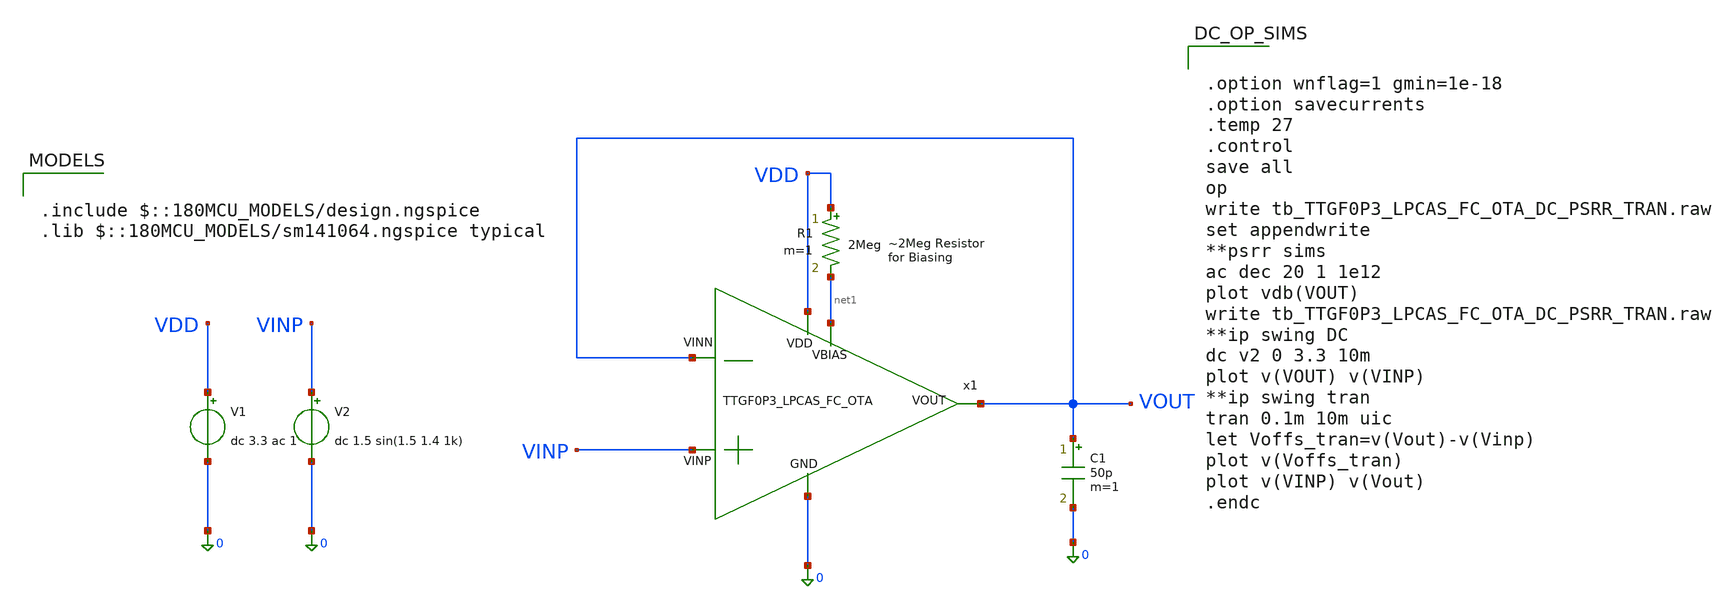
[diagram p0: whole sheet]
** sch_path: SCH/tb_TTGF0P3_LPCAS_FC_OTA_DC_PSRR_TRAN.sch
**.subckt tb_TTGF0P3_LPCAS_FC_OTA_DC_PSRR_TRAN
x1 VDD net1 VOUT VINP VOUT 0 TTGF0P3_LPCAS_FC_OTA
V1 VDD 0 dc 3.3 ac 1
V2 VINP 0 dc 1.5 sin(1.5 1.4 1k)
R1 VDD net1 2Meg m=1
C1 VOUT 0 50p m=1
**** begin user architecture code


.option wnflag=1 gmin=1e-18
.option savecurrents
.temp 27
.control
save all
op
write tb_TTGF0P3_LPCAS_FC_OTA_DC_PSRR_TRAN.raw
set appendwrite
**psrr sims
ac dec 20 1 1e12
plot vdb(VOUT)
write tb_TTGF0P3_LPCAS_FC_OTA_DC_PSRR_TRAN.raw
**ip swing DC
dc v2 0 3.3 10m
plot v(VOUT) v(VINP)
**ip swing tran
tran 0.1m 10m uic
let Voffs_tran=v(Vout)-v(Vinp)
plot v(Voffs_tran)
plot v(VINP) v(Vout)
.endc



.include $::180MCU_MODELS/design.ngspice
.lib $::180MCU_MODELS/sm141064.ngspice typical

**** end user architecture code
**.ends

* expanding   symbol:  /home/nithin/eda/ttgf0p3/TTGF0P3_LPCAS_FC_OTA.sym # of pins=6
** sym_path: SCH/TTGF0P3_LPCAS_FC_OTA.sym
** sch_path: SCH/TTGF0P3_LPCAS_FC_OTA.sch
.subckt TTGF0P3_LPCAS_FC_OTA VDD VBIAS VOUT VINP VINN GND
*.opin VOUT
*.ipin VINP
*.ipin VINN
*.ipin VDD
*.ipin VBIAS
*.ipin GND
XM1 net11 VBIASCN net1 GND nfet_03v3 L=1u W=4u nf=1 ad='int((nf+1)/2) * W/nf * 0.18u' as='int((nf+2)/2) * W/nf * 0.18u'
+ pd='2*int((nf+1)/2) * (W/nf + 0.18u)' ps='2*int((nf+2)/2) * (W/nf + 0.18u)' nrd='0.18u / W' nrs='0.18u / W'
+ sa=0 sb=0 sd=0 m=1
XM2 VOUT VBIASCN net2 GND nfet_03v3 L=1u W=3u nf=1 ad='int((nf+1)/2) * W/nf * 0.18u' as='int((nf+2)/2) * W/nf * 0.18u'
+ pd='2*int((nf+1)/2) * (W/nf + 0.18u)' ps='2*int((nf+2)/2) * (W/nf + 0.18u)' nrd='0.18u / W' nrs='0.18u / W'
+ sa=0 sb=0 sd=0 m=1
XM5 net12 VBIASCP net4 VDD pfet_03v3 L=0.3u W=3u nf=1 ad='int((nf+1)/2) * W/nf * 0.18u' as='int((nf+2)/2) * W/nf * 0.18u'
+ pd='2*int((nf+1)/2) * (W/nf + 0.18u)' ps='2*int((nf+2)/2) * (W/nf + 0.18u)' nrd='0.18u / W' nrs='0.18u / W'
+ sa=0 sb=0 sd=0 m=1
XM6 net5 VBIASCP net3 VDD pfet_03v3 L=0.3u W=3u nf=1 ad='int((nf+1)/2) * W/nf * 0.18u' as='int((nf+2)/2) * W/nf * 0.18u'
+ pd='2*int((nf+1)/2) * (W/nf + 0.18u)' ps='2*int((nf+2)/2) * (W/nf + 0.18u)' nrd='0.18u / W' nrs='0.18u / W'
+ sa=0 sb=0 sd=0 m=1
XM7 net4 net5 net13 VDD pfet_03v3 L=1u W=8u nf=1 ad='int((nf+1)/2) * W/nf * 0.18u' as='int((nf+2)/2) * W/nf * 0.18u'
+ pd='2*int((nf+1)/2) * (W/nf + 0.18u)' ps='2*int((nf+2)/2) * (W/nf + 0.18u)' nrd='0.18u / W' nrs='0.18u / W'
+ sa=0 sb=0 sd=0 m=6
XM8 net3 net5 net14 VDD pfet_03v3 L=1u W=8u nf=1 ad='int((nf+1)/2) * W/nf * 0.18u' as='int((nf+2)/2) * W/nf * 0.18u'
+ pd='2*int((nf+1)/2) * (W/nf + 0.18u)' ps='2*int((nf+2)/2) * (W/nf + 0.18u)' nrd='0.18u / W' nrs='0.18u / W'
+ sa=0 sb=0 sd=0 m=6
XM9 VBIAS VBIAS GND GND nfet_03v3 L=3u W=2u nf=1 ad='int((nf+1)/2) * W/nf * 0.18u' as='int((nf+2)/2) * W/nf * 0.18u'
+ pd='2*int((nf+1)/2) * (W/nf + 0.18u)' ps='2*int((nf+2)/2) * (W/nf + 0.18u)' nrd='0.18u / W' nrs='0.18u / W'
+ sa=0 sb=0 sd=0 m=1
XM10 net9 VBIAS GND GND nfet_03v3 L=3u W=2u nf=1 ad='int((nf+1)/2) * W/nf * 0.18u' as='int((nf+2)/2) * W/nf * 0.18u'
+ pd='2*int((nf+1)/2) * (W/nf + 0.18u)' ps='2*int((nf+2)/2) * (W/nf + 0.18u)' nrd='0.18u / W' nrs='0.18u / W'
+ sa=0 sb=0 sd=0 m=5
XM3 net1 VBIAS GND GND nfet_03v3 L=3u W=2u nf=1 ad='int((nf+1)/2) * W/nf * 0.18u' as='int((nf+2)/2) * W/nf * 0.18u'
+ pd='2*int((nf+1)/2) * (W/nf + 0.18u)' ps='2*int((nf+2)/2) * (W/nf + 0.18u)' nrd='0.18u / W' nrs='0.18u / W'
+ sa=0 sb=0 sd=0 m=1
XM4 net2 VBIAS GND GND nfet_03v3 L=3u W=2u nf=1 ad='int((nf+1)/2) * W/nf * 0.18u' as='int((nf+2)/2) * W/nf * 0.18u'
+ pd='2*int((nf+1)/2) * (W/nf + 0.18u)' ps='2*int((nf+2)/2) * (W/nf + 0.18u)' nrd='0.18u / W' nrs='0.18u / W'
+ sa=0 sb=0 sd=0 m=1
XM14 net10 VBIAS GND GND nfet_03v3 L=3u W=2u nf=1 ad='int((nf+1)/2) * W/nf * 0.18u' as='int((nf+2)/2) * W/nf * 0.18u'
+ pd='2*int((nf+1)/2) * (W/nf + 0.18u)' ps='2*int((nf+2)/2) * (W/nf + 0.18u)' nrd='0.18u / W' nrs='0.18u / W'
+ sa=0 sb=0 sd=0 m=1
XM15 net15 VBIASCP VDD VDD pfet_03v3 L=0.3u W=0.3u nf=1 ad='int((nf+1)/2) * W/nf * 0.18u' as='int((nf+2)/2) * W/nf * 0.18u'
+ pd='2*int((nf+1)/2) * (W/nf + 0.18u)' ps='2*int((nf+2)/2) * (W/nf + 0.18u)' nrd='0.18u / W' nrs='0.18u / W'
+ sa=0 sb=0 sd=0 m=1
Vmeas net3 net7 0
.save i(vmeas)
Vmeas1 net4 net8 0
.save i(vmeas1)
Vmeas2 net6 net9 0
.save i(vmeas2)
Vmeas3 VBIASCP net10 0
.save i(vmeas3)
Vmeas4 net5 net11 0
.save i(vmeas4)
Vmeas5 net12 VOUT 0
.save i(vmeas5)
XM16 net7 VINP net6 GND nfet_03v3 L=1u W=8.5u nf=1 ad='int((nf+1)/2) * W/nf * 0.18u' as='int((nf+2)/2) * W/nf * 0.18u'
+ pd='2*int((nf+1)/2) * (W/nf + 0.18u)' ps='2*int((nf+2)/2) * (W/nf + 0.18u)' nrd='0.18u / W' nrs='0.18u / W'
+ sa=0 sb=0 sd=0 m=4
XM11 net8 VINN net6 GND nfet_03v3 L=1u W=8.5u nf=1 ad='int((nf+1)/2) * W/nf * 0.18u' as='int((nf+2)/2) * W/nf * 0.18u'
+ pd='2*int((nf+1)/2) * (W/nf + 0.18u)' ps='2*int((nf+2)/2) * (W/nf + 0.18u)' nrd='0.18u / W' nrs='0.18u / W'
+ sa=0 sb=0 sd=0 m=4
Vmeas6 VDD net14 0
.save i(vmeas6)
Vmeas7 VDD net13 0
.save i(vmeas7)
C1 VOUT GND 100p m=1
XM12 VBIASCP VBIASCP net15 VDD pfet_03v3 L=0.3u W=0.3u nf=1 ad='int((nf+1)/2) * W/nf * 0.18u' as='int((nf+2)/2) * W/nf * 0.18u'
+ pd='2*int((nf+1)/2) * (W/nf + 0.18u)' ps='2*int((nf+2)/2) * (W/nf + 0.18u)' nrd='0.18u / W' nrs='0.18u / W'
+ sa=0 sb=0 sd=0 m=1
XM17 net16 VBIASCP VDD VDD pfet_03v3 L=0.3u W=0.3u nf=1 ad='int((nf+1)/2) * W/nf * 0.18u' as='int((nf+2)/2) * W/nf * 0.18u'
+ pd='2*int((nf+1)/2) * (W/nf + 0.18u)' ps='2*int((nf+2)/2) * (W/nf + 0.18u)' nrd='0.18u / W' nrs='0.18u / W'
+ sa=0 sb=0 sd=0 m=1
XM18 VBIASCN VBIASCP net16 VDD pfet_03v3 L=0.3u W=0.3u nf=1 ad='int((nf+1)/2) * W/nf * 0.18u' as='int((nf+2)/2) * W/nf * 0.18u'
+ pd='2*int((nf+1)/2) * (W/nf + 0.18u)' ps='2*int((nf+2)/2) * (W/nf + 0.18u)' nrd='0.18u / W' nrs='0.18u / W'
+ sa=0 sb=0 sd=0 m=1
XM19 net17 VBIASCN GND GND nfet_03v3 L=1u W=1u nf=1 ad='int((nf+1)/2) * W/nf * 0.18u' as='int((nf+2)/2) * W/nf * 0.18u'
+ pd='2*int((nf+1)/2) * (W/nf + 0.18u)' ps='2*int((nf+2)/2) * (W/nf + 0.18u)' nrd='0.18u / W' nrs='0.18u / W'
+ sa=0 sb=0 sd=0 m=1
XM20 net18 VBIASCN net17 GND nfet_03v3 L=1u W=1u nf=1 ad='int((nf+1)/2) * W/nf * 0.18u' as='int((nf+2)/2) * W/nf * 0.18u'
+ pd='2*int((nf+1)/2) * (W/nf + 0.18u)' ps='2*int((nf+2)/2) * (W/nf + 0.18u)' nrd='0.18u / W' nrs='0.18u / W'
+ sa=0 sb=0 sd=0 m=1
XM21 VBIASCN VBIASCN net18 GND nfet_03v3 L=1u W=1u nf=1 ad='int((nf+1)/2) * W/nf * 0.18u' as='int((nf+2)/2) * W/nf * 0.18u'
+ pd='2*int((nf+1)/2) * (W/nf + 0.18u)' ps='2*int((nf+2)/2) * (W/nf + 0.18u)' nrd='0.18u / W' nrs='0.18u / W'
+ sa=0 sb=0 sd=0 m=1
.ends

.end
